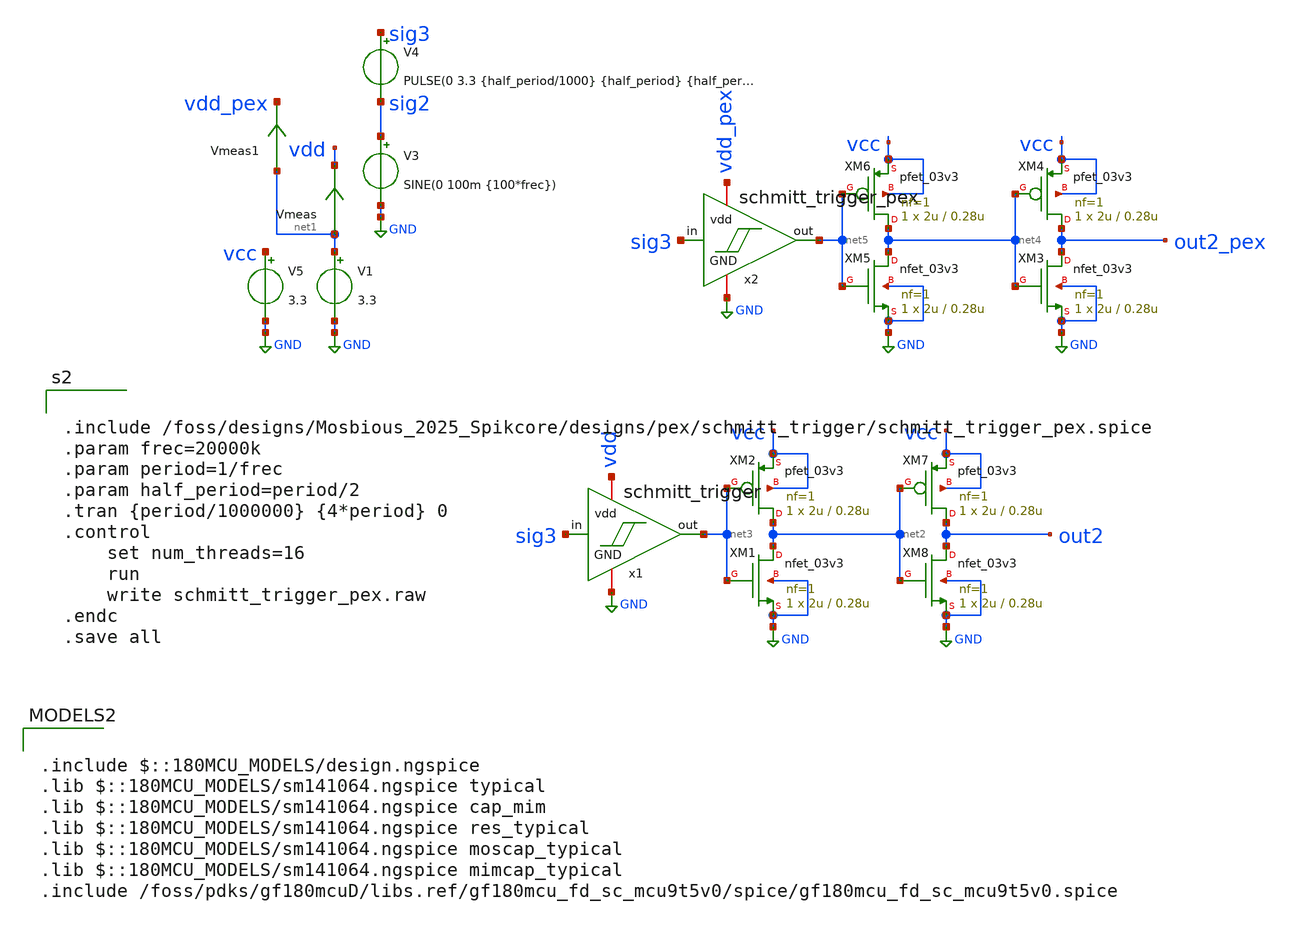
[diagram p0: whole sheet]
** sch_path: designs/pex/schmitt_trigger/schmitt_trigger.sch
**.subckt schmitt_trigger
V1 net1 GND 3.3
x1 net3 sig3 vdd GND schmitt_trigger
V3 sig2 GND SINE(0 100m {100*frec})
V4 sig3 sig2 PULSE(0 3.3 {half_period/1000} {half_period} {half_period} {half_period/1000} {period})
XM8 out2 net2 GND GND nfet_03v3 L=0.28u W=2u nf=1 ad='int((nf+1)/2) * W/nf * 0.18u' as='int((nf+2)/2) * W/nf * 0.18u'
+ pd='2*int((nf+1)/2) * (W/nf + 0.18u)' ps='2*int((nf+2)/2) * (W/nf + 0.18u)' nrd='0.18u / W' nrs='0.18u / W'
+ sa=0 sb=0 sd=0 m=1
XM7 out2 net2 vcc vcc pfet_03v3 L=0.28u W=2u nf=1 ad='int((nf+1)/2) * W/nf * 0.18u' as='int((nf+2)/2) * W/nf * 0.18u'
+ pd='2*int((nf+1)/2) * (W/nf + 0.18u)' ps='2*int((nf+2)/2) * (W/nf + 0.18u)' nrd='0.18u / W' nrs='0.18u / W'
+ sa=0 sb=0 sd=0 m=1
XM1 net2 net3 GND GND nfet_03v3 L=0.28u W=2u nf=1 ad='int((nf+1)/2) * W/nf * 0.18u' as='int((nf+2)/2) * W/nf * 0.18u'
+ pd='2*int((nf+1)/2) * (W/nf + 0.18u)' ps='2*int((nf+2)/2) * (W/nf + 0.18u)' nrd='0.18u / W' nrs='0.18u / W'
+ sa=0 sb=0 sd=0 m=1
XM2 net2 net3 vcc vcc pfet_03v3 L=0.28u W=2u nf=1 ad='int((nf+1)/2) * W/nf * 0.18u' as='int((nf+2)/2) * W/nf * 0.18u'
+ pd='2*int((nf+1)/2) * (W/nf + 0.18u)' ps='2*int((nf+2)/2) * (W/nf + 0.18u)' nrd='0.18u / W' nrs='0.18u / W'
+ sa=0 sb=0 sd=0 m=1
Vmeas net1 vdd 0
.save i(vmeas)
V5 vcc GND 3.3
x2 net5 sig3 vdd_pex GND schmitt_trigger_pex
XM3 out2_pex net4 GND GND nfet_03v3 L=0.28u W=2u nf=1 ad='int((nf+1)/2) * W/nf * 0.18u' as='int((nf+2)/2) * W/nf * 0.18u'
+ pd='2*int((nf+1)/2) * (W/nf + 0.18u)' ps='2*int((nf+2)/2) * (W/nf + 0.18u)' nrd='0.18u / W' nrs='0.18u / W'
+ sa=0 sb=0 sd=0 m=1
XM4 out2_pex net4 vcc vcc pfet_03v3 L=0.28u W=2u nf=1 ad='int((nf+1)/2) * W/nf * 0.18u' as='int((nf+2)/2) * W/nf * 0.18u'
+ pd='2*int((nf+1)/2) * (W/nf + 0.18u)' ps='2*int((nf+2)/2) * (W/nf + 0.18u)' nrd='0.18u / W' nrs='0.18u / W'
+ sa=0 sb=0 sd=0 m=1
XM5 net4 net5 GND GND nfet_03v3 L=0.28u W=2u nf=1 ad='int((nf+1)/2) * W/nf * 0.18u' as='int((nf+2)/2) * W/nf * 0.18u'
+ pd='2*int((nf+1)/2) * (W/nf + 0.18u)' ps='2*int((nf+2)/2) * (W/nf + 0.18u)' nrd='0.18u / W' nrs='0.18u / W'
+ sa=0 sb=0 sd=0 m=1
XM6 net4 net5 vcc vcc pfet_03v3 L=0.28u W=2u nf=1 ad='int((nf+1)/2) * W/nf * 0.18u' as='int((nf+2)/2) * W/nf * 0.18u'
+ pd='2*int((nf+1)/2) * (W/nf + 0.18u)' ps='2*int((nf+2)/2) * (W/nf + 0.18u)' nrd='0.18u / W' nrs='0.18u / W'
+ sa=0 sb=0 sd=0 m=1
Vmeas1 net1 vdd_pex 0
.save i(vmeas1)
**** begin user architecture code

.include $::180MCU_MODELS/design.ngspice
.lib $::180MCU_MODELS/sm141064.ngspice typical
.lib $::180MCU_MODELS/sm141064.ngspice cap_mim
.lib $::180MCU_MODELS/sm141064.ngspice res_typical
.lib $::180MCU_MODELS/sm141064.ngspice moscap_typical
.lib $::180MCU_MODELS/sm141064.ngspice mimcap_typical
.include /foss/pdks/gf180mcuD/libs.ref/gf180mcu_fd_sc_mcu9t5v0/spice/gf180mcu_fd_sc_mcu9t5v0.spice



.include /foss/designs/Mosbious_2025_Spikcore/designs/pex/schmitt_trigger/schmitt_trigger_pex.spice
.param frec=20000k
.param period=1/frec
.param half_period=period/2
.tran {period/1000000} {4*period} 0
.control
	set num_threads=16
	run
	write schmitt_trigger_pex.raw
.endc
.save all


**** end user architecture code
**.ends
.GLOBAL GND
.end
